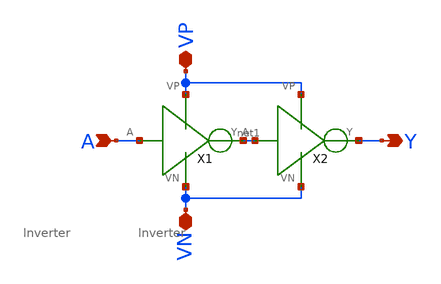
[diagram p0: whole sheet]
** sch_path: buffer.sch
**.subckt buffer A VP VN Y
*.ipin A
*.iopin VP
*.iopin VN
*.opin Y
X1 A net1 VP VN Inverter
X2 net1 Y VP VN Inverter
**.ends

* expanding   symbol:  Inverter.sym # of pins=4
** sym_path: Inverter.sym
** sch_path: Inverter.sch
.subckt Inverter A Y VP VN
*.ipin A
*.iopin VP
*.opin Y
*.iopin VN
XM1 Y A VN VN sky130_fd_pr__nfet_01v8 L=0.15 W=1 nf=1 ad='int((nf+1)/2) * W/nf * 0.29' as='int((nf+2)/2) * W/nf * 0.29'
+ pd='2*int((nf+1)/2) * (W/nf + 0.29)' ps='2*int((nf+2)/2) * (W/nf + 0.29)' nrd='0.29 / W' nrs='0.29 / W'
+ sa=0 sb=0 sd=0 mult=1 m=1
XM3 Y A VP VP sky130_fd_pr__pfet_01v8 L=0.15 W=1 nf=1 ad='int((nf+1)/2) * W/nf * 0.29' as='int((nf+2)/2) * W/nf * 0.29'
+ pd='2*int((nf+1)/2) * (W/nf + 0.29)' ps='2*int((nf+2)/2) * (W/nf + 0.29)' nrd='0.29 / W' nrs='0.29 / W'
+ sa=0 sb=0 sd=0 mult=1 m=1
.ends

.end
